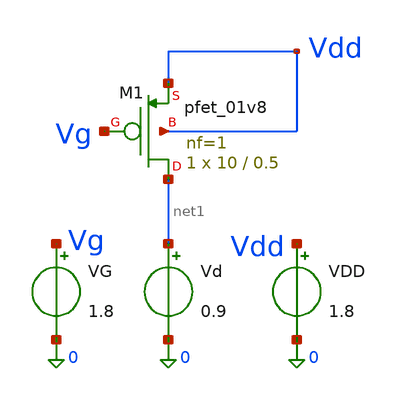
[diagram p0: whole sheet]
** sch_path: characterization/Schematics/pmos_characterization.sch
**.subckt pmos_characterization
XM1 net1 Vg Vdd Vdd sky130_fd_pr__pfet_01v8 L=0.5 W=10 nf=1 ad='int((1 + 1)/2) * 10 / 1 * 0.29' as='int((1 + 2)/2) * 10 / 1 * 0.29'
+ pd='2*int((1 + 1)/2) * (10 / 1 + 0.29)' ps='2*int((1 + 2)/2) * (10 / 1 + 0.29)' nrd='0.29 / 10 ' nrs='0.29 / 10 '
+ sa=0 sb=0 sd=0 mult=1 m=1
VDD Vdd 0 1.8
.save i(vdd)
VG Vg 0 1.8
Vd net1 0 0.9
**** begin user architecture code

** opencircuitdesign pdks install
.lib $::SKYWATER_MODELS/sky130.lib.spice tt


.options savecurrents

.control
    save all

    * =====================================================
    * PMOS gm/Id characterization
    * VS = VB = 1.8 V
    * W = 10 um
    * L = 0.5 um
    * =====================================================

    * CASE 1: VSD = 1.8 V
    alter Vd 0
    dc Vg 1.8 0 -0.001

    let id = abs(Vd#branch)
    let gm = -deriv(id)
    let gm_id = gm / id
    let id_w = id / 10e-6


    * CASE 2: VSD = 0.9 V
    alter Vd 0.9
    dc Vg 1.8 0 -0.001

    let id = abs(Vd#branch)
    let gm = -deriv(id)
    let gm_id = gm / id
    let id_w = id / 10e-6


    * CASE 3: VSD = 0.6 V
    alter Vd 1.2
    dc Vg 1.8 0 -0.001

    let id = abs(Vd#branch)
    let gm = -deriv(id)
    let gm_id = gm / id
    let id_w = id / 10e-6


    * CASE 4: VSD = 0.3 V
    alter Vd 1.5
    dc Vg 1.8 0 -0.001

    let id = abs(Vd#branch)
    let gm = -deriv(id)
    let gm_id = gm / id
    let id_w = id / 10e-6


    * =====================================================
    * Copy results to const for friendly legend names
    * =====================================================

    setplot const

    let vsd_1v8 = dc1.gm_id
    let idw_1v8 = dc1.id_w

    let vsd_0v9 = dc2.gm_id
    let idw_0v9 = dc2.id_w

    let vsd_0v6 = dc3.gm_id
    let idw_0v6 = dc3.id_w

    let vsd_0v3 = dc4.gm_id
    let idw_0v3 = dc4.id_w


    * IMPORTANT: keep this plot command on ONE LINE
    plot vsd_1v8 vs idw_1v8 vsd_0v9 vs idw_0v9 vsd_0v6 vs idw_0v6 vsd_0v3 vs idw_0v3 xlog xlabel 'Id/W [uA/um]'
+ ylabel 'gm/Id [1/V]' title 'PMOS gm/Id Characterization'

.endc

**** end user architecture code
**.ends
.end
